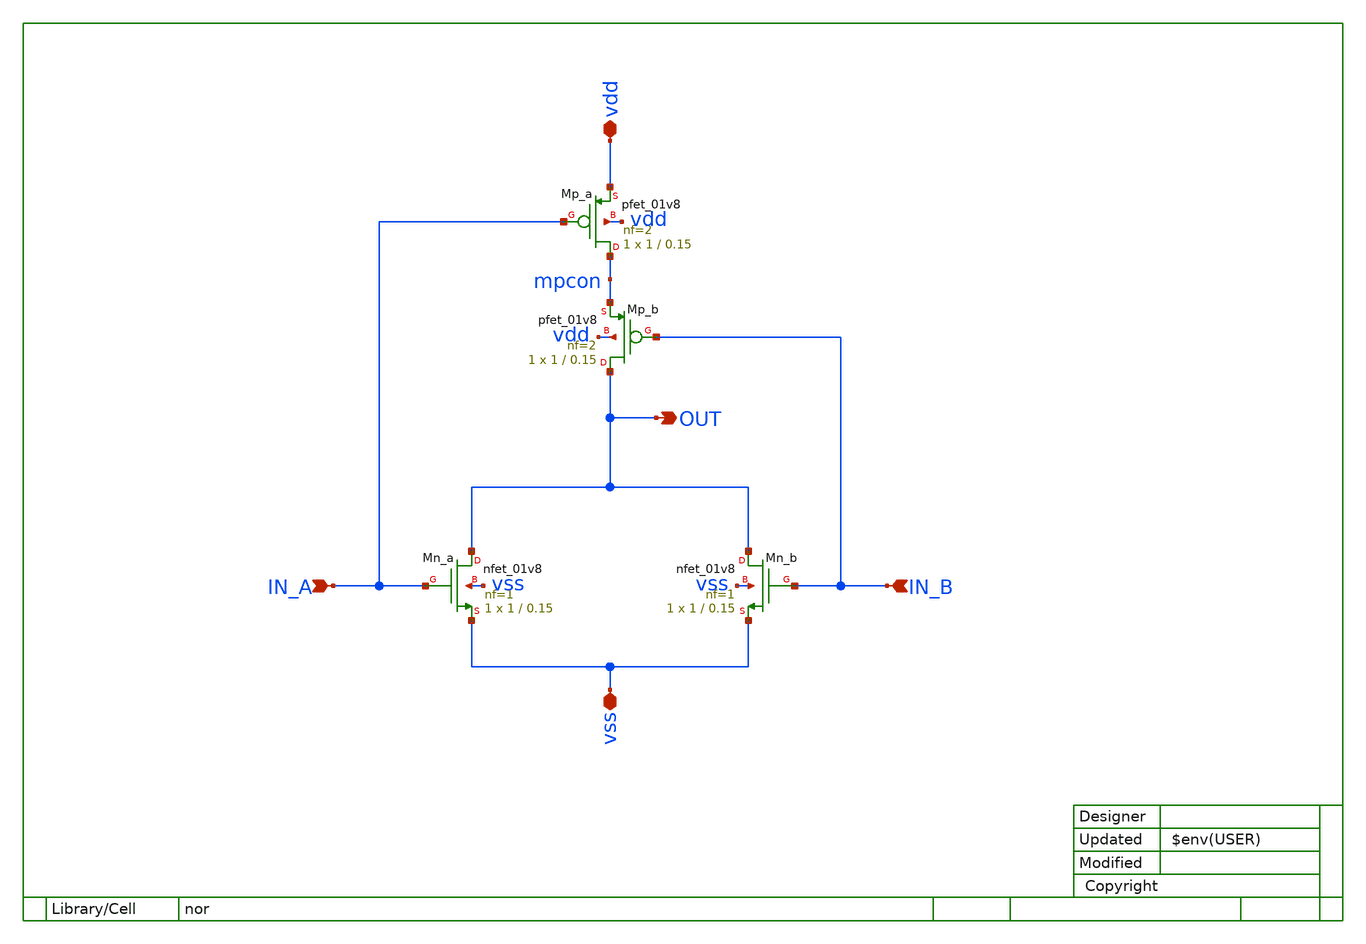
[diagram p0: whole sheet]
** sch_path: xsch/ip/logic/nor.sch
**.subckt nor IN_A OUT vss vdd IN_B
*.ipin IN_A
*.opin OUT
*.iopin vss
*.iopin vdd
*.ipin IN_B
XMn_a OUT IN_A vss vss sky130_fd_pr__nfet_01v8 L=0.15 W=1 nf=1 ad='int((1 + 1)/2) * 1 / 1 * 0.29' as='int((1 + 2)/2) * 1 / 1 * 0.29'
+ pd='2*int((1 + 1)/2) * (1 / 1 + 0.29)' ps='2*int((1 + 2)/2) * (1 / 1 + 0.29)' nrd='0.29 / 1 ' nrs='0.29 / 1 '
+ sa=0 sb=0 sd=0 mult=1 m=1
XMp_a mpcon IN_A vdd vdd sky130_fd_pr__pfet_01v8 L=0.15 W=1 nf=2 ad='int((nf+1)/2) * W/nf * 0.29' as='int((nf+2)/2) * W/nf * 0.29'
+ pd='2*int((nf+1)/2) * (W/nf + 0.29)' ps='2*int((nf+2)/2) * (W/nf + 0.29)' nrd='0.29 / W' nrs='0.29 / W'
+ sa=0 sb=0 sd=0 mult=1 m=1
XMp_b OUT IN_B mpcon vdd sky130_fd_pr__pfet_01v8 L=0.15 W=1 nf=2 ad='int((nf+1)/2) * W/nf * 0.29' as='int((nf+2)/2) * W/nf * 0.29'
+ pd='2*int((nf+1)/2) * (W/nf + 0.29)' ps='2*int((nf+2)/2) * (W/nf + 0.29)' nrd='0.29 / W' nrs='0.29 / W'
+ sa=0 sb=0 sd=0 mult=1 m=1
XMn_b OUT IN_B vss vss sky130_fd_pr__nfet_01v8 L=0.15 W=1 nf=1 ad='int((1 + 1)/2) * 1 / 1 * 0.29' as='int((1 + 2)/2) * 1 / 1 * 0.29'
+ pd='2*int((1 + 1)/2) * (1 / 1 + 0.29)' ps='2*int((1 + 2)/2) * (1 / 1 + 0.29)' nrd='0.29 / 1 ' nrs='0.29 / 1 '
+ sa=0 sb=0 sd=0 mult=1 m=1
**.ends
.end
